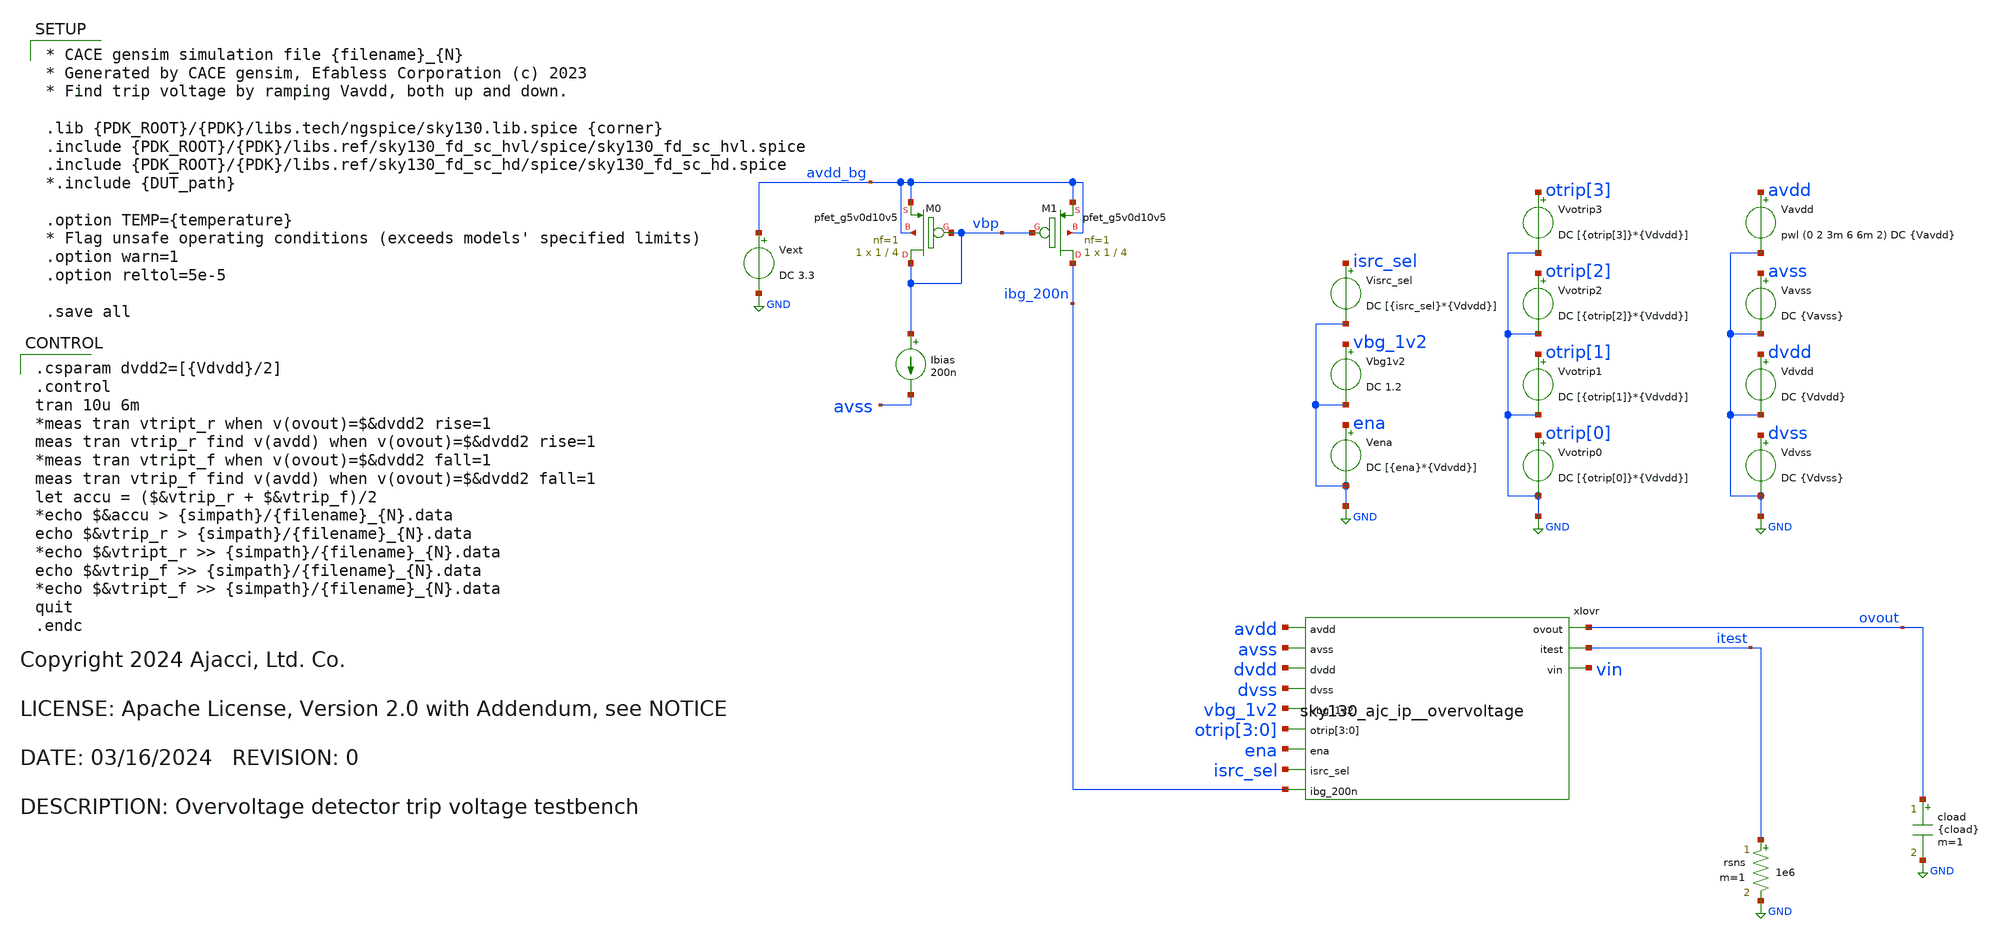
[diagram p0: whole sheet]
** sch_path: cace/trip_up_down.sch
* Copyright 2024 Ajacci, Ltd. Co.
* LICENSE: Apache License, Version 2.0 with Addendum, see NOTICE
**.subckt trip_up_down
Vavss avss GND DC {Vavss}
Vena ena GND DC [{ena}*{Vdvdd}]
Vavdd avdd GND pwl (0 2 3m 6 6m 2) DC {Vavdd}
.save i(vavdd)
Vbg1v2 vbg_1v2 GND DC 1.2
Ibias vbp avss 200n
XM1 ibg_200n vbp avdd_bg avdd_bg sky130_fd_pr__pfet_g5v0d10v5 L=4 W=1 nf=1 ad='int((nf+1)/2) * W/nf * 0.29'
+ as='int((nf+2)/2) * W/nf * 0.29' pd='2*int((nf+1)/2) * (W/nf + 0.29)' ps='2*int((nf+2)/2) * (W/nf + 0.29)'
+ nrd='0.29 / W' nrs='0.29 / W' sa=0 sb=0 sd=0 mult=1 m=1
XM0 vbp vbp avdd_bg avdd_bg sky130_fd_pr__pfet_g5v0d10v5 L=4 W=1 nf=1 ad='int((nf+1)/2) * W/nf * 0.29'
+ as='int((nf+2)/2) * W/nf * 0.29' pd='2*int((nf+1)/2) * (W/nf + 0.29)' ps='2*int((nf+2)/2) * (W/nf + 0.29)'
+ nrd='0.29 / W' nrs='0.29 / W' sa=0 sb=0 sd=0 mult=1 m=1
Vdvss dvss GND DC {Vdvss}
Vdvdd dvdd GND DC {Vdvdd}
.save i(vdvdd)
rsns itest GND 1e6 m=1
cload ovout GND {cload} m=1
xIovr avdd avss dvdd dvss vbg_1v2 ovout itest otrip[3] otrip[2] otrip[1] otrip[0] vin ena isrc_sel
+ ibg_200n sky130_ajc_ip__overvoltage
Vvotrip0 otrip[0] GND DC [{otrip[0]}*{Vdvdd}]
.save i(vvotrip0)
Vvotrip1 otrip[1] GND DC [{otrip[1]}*{Vdvdd}]
.save i(vvotrip1)
Vvotrip2 otrip[2] GND DC [{otrip[2]}*{Vdvdd}]
.save i(vvotrip2)
Vvotrip3 otrip[3] GND DC [{otrip[3]}*{Vdvdd}]
.save i(vvotrip3)
Visrc_sel isrc_sel GND DC [{isrc_sel}*{Vdvdd}]
Vext avdd_bg GND DC 3.3
.save i(vext)
**** begin user architecture code

* CACE gensim simulation file {filename}_{N}
* Generated by CACE gensim, Efabless Corporation (c) 2023
* Find trip voltage by ramping Vavdd, both up and down.

.lib {PDK_ROOT}/{PDK}/libs.tech/ngspice/sky130.lib.spice {corner}
.include {PDK_ROOT}/{PDK}/libs.ref/sky130_fd_sc_hvl/spice/sky130_fd_sc_hvl.spice
.include {PDK_ROOT}/{PDK}/libs.ref/sky130_fd_sc_hd/spice/sky130_fd_sc_hd.spice
*.include {DUT_path}

.option TEMP={temperature}
* Flag unsafe operating conditions (exceeds models' specified limits)
.option warn=1
.option reltol=5e-5

.save all



.csparam dvdd2=[{Vdvdd}/2]
.control
tran 10u 6m
*meas tran vtript_r when v(ovout)=$&dvdd2 rise=1
meas tran vtrip_r find v(avdd) when v(ovout)=$&dvdd2 rise=1
*meas tran vtript_f when v(ovout)=$&dvdd2 fall=1
meas tran vtrip_f find v(avdd) when v(ovout)=$&dvdd2 fall=1
let accu = ($&vtrip_r + $&vtrip_f)/2
*echo $&accu > {simpath}/{filename}_{N}.data
echo $&vtrip_r > {simpath}/{filename}_{N}.data
*echo $&vtript_r >> {simpath}/{filename}_{N}.data
echo $&vtrip_f >> {simpath}/{filename}_{N}.data
*echo $&vtript_f >> {simpath}/{filename}_{N}.data
quit
.endc


**** end user architecture code
**.ends
.GLOBAL GND
.end
